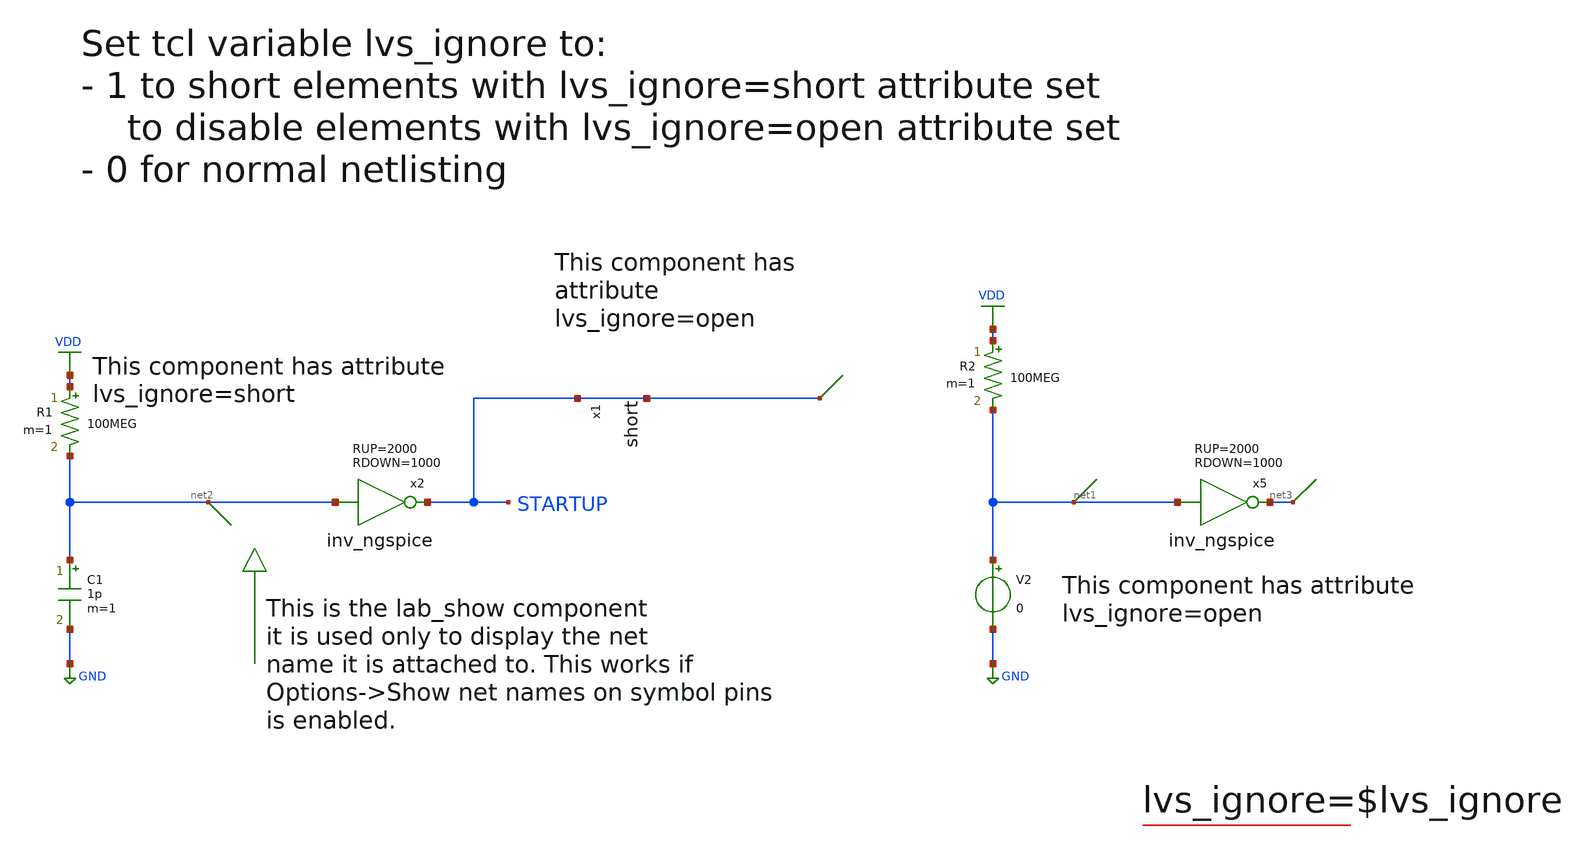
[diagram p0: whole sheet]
** sch_path: tests/test_sweep_diff/examples/test_lvs_ignore/schematic/test_lvs_ignore.sch
* Copyright (C) 1998-2024 Stefan Frederik Schippers
* This program is free software; you can redistribute it and/or modify
* it under the terms of the GNU General Public License as published by
* the Free Software Foundation; either version 2 of the License, or
* (at your option) any later version.
* This program is distributed in the hope that it will be useful,
* but WITHOUT ANY WARRANTY; without even the implied warranty of
* MERCHANTABILITY or FITNESS FOR A PARTICULAR PURPOSE.  See the
* GNU General Public License for more details.
* You should have received a copy of the GNU General Public License
* along with this program; if not, write to the Free Software
**.subckt test_lvs_ignore
V2 net1 GND 0
x5 net3 net1 inv_ngspice RUP=2000 RDOWN=1000
R1 VDD net2 100MEG m=1
C1 net2 GND 1p m=1
x2 STARTUP net2 inv_ngspice RUP=2000 RDOWN=1000
R2 VDD net1 100MEG m=1
* short x1 : STARTUP <--> STARTUP
**.ends
.GLOBAL GND
.GLOBAL VDD
.end
